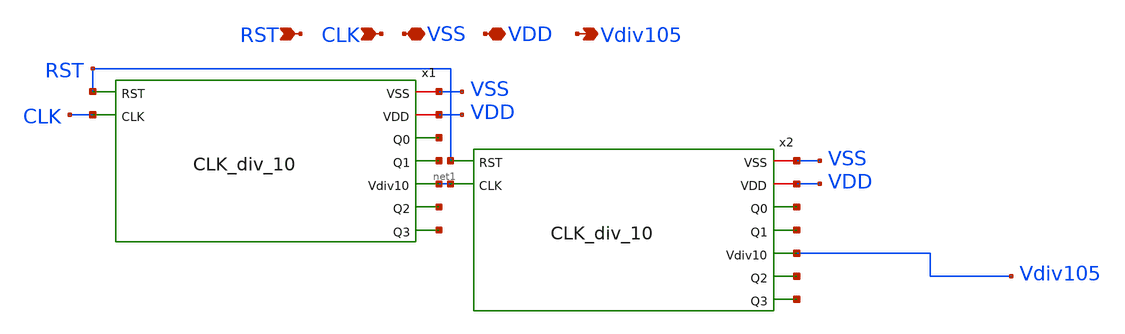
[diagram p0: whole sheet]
** sch_path: Clock_Generator_PAKISTAN_02/Schematics/CLK_div_105.sch
**.subckt CLK_div_105 CLK VSS VDD RST Vdiv105
*.ipin CLK
*.iopin VSS
*.iopin VDD
*.ipin RST
*.opin Vdiv105
x1 VSS VDD net2 net3 RST net1 net4 net5 CLK CLK_div_10
x2 VSS VDD net6 net7 RST Vdiv105 net8 net9 net1 CLK_div_10
**.ends
.end
